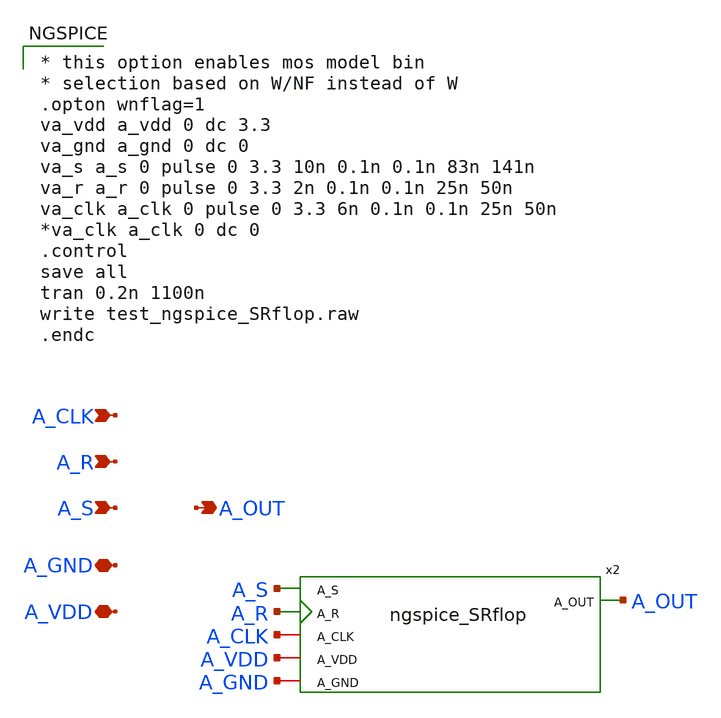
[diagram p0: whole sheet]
** sch_path: xschem/test_ngspice_SRflop.sch
**.subckt test_ngspice_SRflop A_VDD A_S A_GND A_R A_OUT A_CLK
*.iopin A_VDD
*.ipin A_S
*.iopin A_GND
*.ipin A_R
*.opin A_OUT
*.ipin A_CLK
x2 A_OUT A_S A_R A_CLK A_GND A_VDD ngspice_SRflop
**** begin user architecture code

* this option enables mos model bin
* selection based on W/NF instead of W
.opton wnflag=1
va_vdd a_vdd 0 dc 3.3
va_gnd a_gnd 0 dc 0
va_s a_s 0 pulse 0 3.3 10n 0.1n 0.1n 83n 141n
va_r a_r 0 pulse 0 3.3 2n 0.1n 0.1n 25n 50n
va_clk a_clk 0 pulse 0 3.3 6n 0.1n 0.1n 25n 50n
*va_clk a_clk 0 dc 0
.control
save all
tran 0.2n 1100n
write test_ngspice_SRflop.raw
.endc


**** end user architecture code
**.ends

* expanding   symbol:  /foss/designs/TO202406_CMOSVCO_Esm22/xschem/ngspice_SRflop.sym # of pins=6
** sym_path: xschem/ngspice_SRflop.sym
** sch_path: xschem/ngspice_SRflop.sch
.subckt ngspice_SRflop A_OUT A_S A_R A_CLK A_GND A_VDD
*.iopin A_VDD
*.ipin A_S
*.opin A_OUT
*.ipin A_R
*.ipin A_CLK
*.iopin A_GND
* noconn A_VDD
* noconn A_S
* noconn A_R
* noconn A_GND
* noconn A_OUT
* noconn A_CLK
**** begin user architecture code
.model todig_3v3 adc_bridge(in_high=2.2 in_low=1.1  rise_delay=2n fall_delay=2n)
.model toana_3v3 dac_bridge(out_high=3.3 out_low=0)

.model dsrflop d_srff(ic=0 rise_delay=1n fall_delay=1n)

AA2D1 [A_GND] [d_gnd] todig_3v3

AA2D2 [A_S] [d_s] todig_3v3
AA2D3 [A_R] [d_r] todig_3v3
AA2D4 [A_CLK] [d_clk] todig_3v3

A1 d_s d_r d_clk d_gnd d_gnd d_out NULL dsrflop

AD2A1 [d_out] [A_OUT] toana_3v3

**** end user architecture code
.ends

.end
